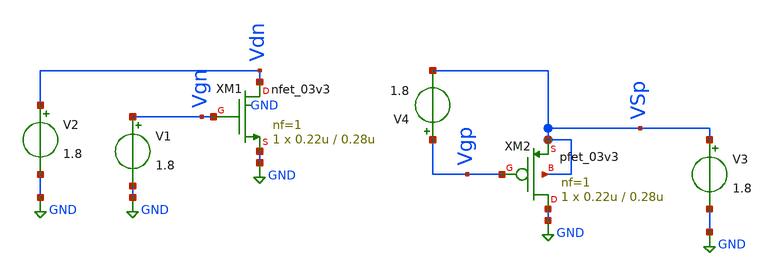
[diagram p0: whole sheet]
** sch_path: xschem/caracterizador/charac.sch
* Copyright 2022 GlobalFoundries PDK Authors
* Licensed under the Apache License, Version 2.0 (the "License");
* you may not use this file except in compliance with the License.
* You may obtain a copy of the License at
* https://www.apache.org/licenses/LICENSE-2.0
* Unless required by applicable law or agreed to in writing, software
* distributed under the License is distributed on an "AS IS" BASIS,
* WITHOUT WARRANTIES OR CONDITIONS OF ANY KIND, either express or implied.
* See the License for the specific language governing permissions and
* limitations under the License.
**.subckt charac
XM1 Vdn Vgn GND GND nfet_03v3 L=0.28u W=0.22u nf=1 ad='int((nf+1)/2) * W/nf * 0.18u' as='int((nf+2)/2) * W/nf * 0.18u'
+ pd='2*int((nf+1)/2) * (W/nf + 0.18u)' ps='2*int((nf+2)/2) * (W/nf + 0.18u)' nrd='0.18u / W' nrs='0.18u / W'
+ sa=0 sb=0 sd=0 m=1 par=1
XM2 GND Vgp VSp VSp pfet_03v3 L=0.28u W=0.22u nf=1 ad='int((nf+1)/2) * W/nf * 0.18u' as='int((nf+2)/2) * W/nf * 0.18u'
+ pd='2*int((nf+1)/2) * (W/nf + 0.18u)' ps='2*int((nf+2)/2) * (W/nf + 0.18u)' nrd='0.18u / W' nrs='0.18u / W'
+ sa=0 sb=0 sd=0 m=1 par=1
V1 Vgn GND 1.8
V2 Vdn GND 1.8
V3 VSp GND 1.8
V4 Vgp VSp 1.8
**** begin user architecture code


.include /home/ringosinye/eda/pdks/gf180mcuD/libs.tech/ngspice/design.ngspice
.lib /home/ringosinye/eda/pdks/gf180mcuD/libs.tech/ngspice/sm141064.ngspice typical
.param sw_stat_mismatch = 0




.control
  save all

  * Coloración de gráficas
  set color0 = white
  set color1 = black
  set color2 = blue
  set color3 = red
  set xbrushwidth = 2

  * ========================================================
  * 1. CAPACITANCIA DE COMPUERTA NMOS (VDS = 1.65V, VGS = 1.65V)
  * ========================================================
  alter V2 = 1.65
  alter V1 = 1.65
  alter V1 acmag = 1

  * Barrido AC de 1 kHz a 100 MHz (1 MHz queda holgadamente dentro)
  ac dec 10 1k 100M
  let cgg_n = imag(-i(V1)) / (2 * pi * frequency)
  meas ac cgg_n_val find cgg_n at = 1meg

  * ========================================================
  * 2. CAPACITANCIA DE COMPUERTA PMOS (VSD = 1.65V, VGS = -1.65V)
  * ========================================================
  alter V3 = 1.65
  alter V4 = -1.65
  alter V4 acmag = 1

  ac dec 10 1k 100M
  let cgg_p = imag(-i(V4)) / (2 * pi * frequency)
  meas ac cgg_p_val find cgg_p at = 1meg

* --- GRAFICAR CAPACITANCIAS VS FRECUENCIA ---
plot ac1.cgg_n ac2.cgg_p xlog title 'Capacitancia de Compuerta Cgg vs Frecuencia' xlabel 'Frecuencia (Hz)'
+ ylabel 'Cgg (F)'

  * --- IMPRIMIR CAPACITANCIAS ---
  echo ================ CAPACITANCIAS DE COMPUERTA (Cgg @ 1MHz) ================
  print ac1.cgg_n_val ac2.cgg_p_val
  echo =========================================================================
.endc


**** end user architecture code
**.ends
.GLOBAL GND
.end
